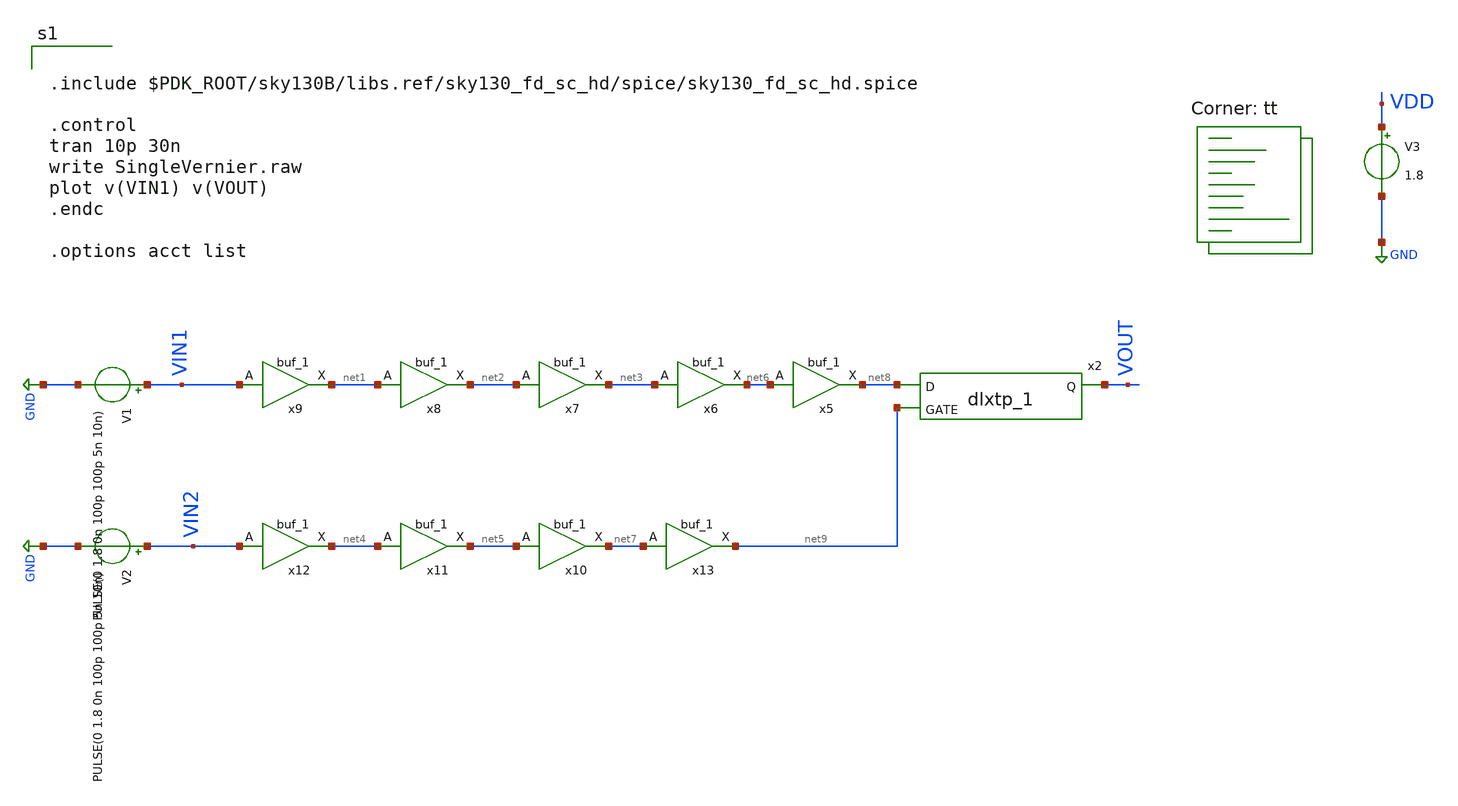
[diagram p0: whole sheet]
** sch_path: xschem/projects/SingleVernier.sch
* Copyright 2021 Stefan Frederik Schippers
* Licensed under the Apache License, Version 2.0 (the "License");
* you may not use this file except in compliance with the License.
* You may obtain a copy of the License at
* https://www.apache.org/licenses/LICENSE-2.0
* Unless required by applicable law or agreed to in writing, software
* distributed under the License is distributed on an "AS IS" BASIS,
* WITHOUT WARRANTIES OR CONDITIONS OF ANY KIND, either express or implied.
* See the License for the specific language governing permissions and
* limitations under the License.
**.subckt SingleVernier
V1 VIN1 GND PULSE(0 1.8 0n 100p 100p 5n 10n)
V2 VIN2 GND PULSE(0 1.8 0n 100p 100p 5n 10n)
V3 VDD GND 1.8
x2 net8 net9 0 0 VDD VDD VOUT sky130_fd_sc_hd__dlxtp_1
x10 net5 GND GND VDD VDD net7 sky130_fd_sc_hd__buf_1
x11 net4 GND GND VDD VDD net5 sky130_fd_sc_hd__buf_1
x12 VIN2 GND GND VDD VDD net4 sky130_fd_sc_hd__buf_1
x6 net3 GND GND VDD VDD net6 sky130_fd_sc_hd__buf_1
x7 net2 GND GND VDD VDD net3 sky130_fd_sc_hd__buf_1
x8 net1 GND GND VDD VDD net2 sky130_fd_sc_hd__buf_1
x9 VIN1 GND GND VDD VDD net1 sky130_fd_sc_hd__buf_1
x5 net6 GND GND VDD VDD net8 sky130_fd_sc_hd__buf_1
x13 net7 GND GND VDD VDD net9 sky130_fd_sc_hd__buf_1
**** begin user architecture code


.include $PDK_ROOT/sky130B/libs.ref/sky130_fd_sc_hd/spice/sky130_fd_sc_hd.spice

.control
tran 10p 30n
write SingleVernier.raw
plot v(VIN1) v(VOUT)
.endc

.options acct list


.lib $::SKYWATER_MODELS/sky130.lib.spice tt
**** end user architecture code
**.ends
.GLOBAL GND
.end
